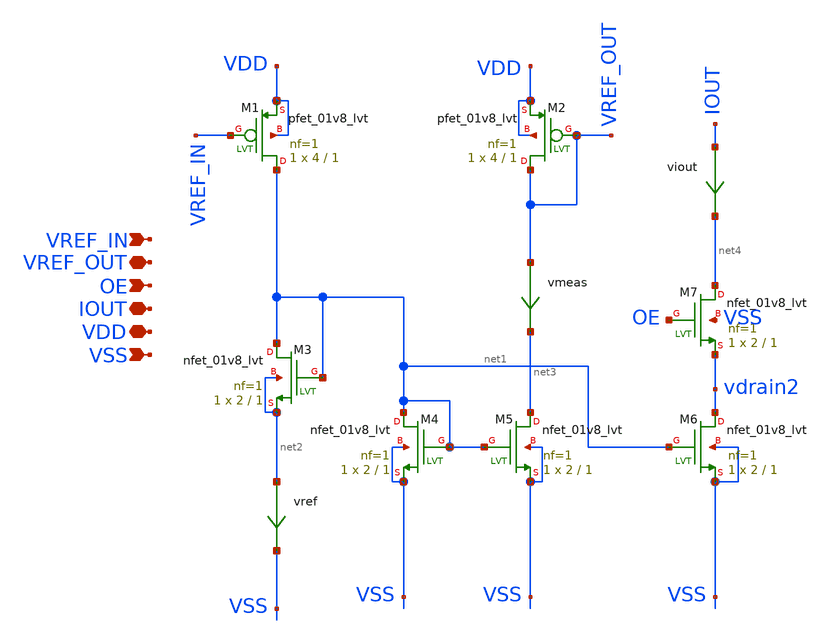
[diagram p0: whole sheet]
** sch_path: tt_um_emilian_rf_playground/xschem/idac1cell.sch
**.subckt idac1cell VSS VREF_OUT VREF_IN VDD IOUT OE
*.ipin VSS
*.iopin VREF_OUT
*.ipin VREF_IN
*.iopin VDD
*.iopin IOUT
*.ipin OE
XM3 net1 net1 net2 net2 sky130_fd_pr__nfet_01v8_lvt L=1 W=2 nf=1 ad='int((nf+1)/2) * W/nf * 0.29' as='int((nf+2)/2) * W/nf * 0.29'
+ pd='2*int((nf+1)/2) * (W/nf + 0.29)' ps='2*int((nf+2)/2) * (W/nf + 0.29)' nrd='0.29 / W' nrs='0.29 / W'
+ sa=0 sb=0 sd=0 mult=1 m=1
XM4 net1 net1 VSS VSS sky130_fd_pr__nfet_01v8_lvt L=1 W=2 nf=1 ad='int((nf+1)/2) * W/nf * 0.29' as='int((nf+2)/2) * W/nf * 0.29'
+ pd='2*int((nf+1)/2) * (W/nf + 0.29)' ps='2*int((nf+2)/2) * (W/nf + 0.29)' nrd='0.29 / W' nrs='0.29 / W'
+ sa=0 sb=0 sd=0 mult=1 m=1
XM1 net1 VREF_IN VDD VDD sky130_fd_pr__pfet_01v8_lvt L=1 W=4 nf=1 ad='int((nf+1)/2) * W/nf * 0.29' as='int((nf+2)/2) * W/nf * 0.29'
+ pd='2*int((nf+1)/2) * (W/nf + 0.29)' ps='2*int((nf+2)/2) * (W/nf + 0.29)' nrd='0.29 / W' nrs='0.29 / W'
+ sa=0 sb=0 sd=0 mult=1 m=1
XM5 net3 net1 VSS VSS sky130_fd_pr__nfet_01v8_lvt L=1 W=2 nf=1 ad='int((nf+1)/2) * W/nf * 0.29' as='int((nf+2)/2) * W/nf * 0.29'
+ pd='2*int((nf+1)/2) * (W/nf + 0.29)' ps='2*int((nf+2)/2) * (W/nf + 0.29)' nrd='0.29 / W' nrs='0.29 / W'
+ sa=0 sb=0 sd=0 mult=1 m=1
XM2 VREF_OUT VREF_OUT VDD VDD sky130_fd_pr__pfet_01v8_lvt L=1 W=4 nf=1 ad='int((nf+1)/2) * W/nf * 0.29'
+ as='int((nf+2)/2) * W/nf * 0.29' pd='2*int((nf+1)/2) * (W/nf + 0.29)' ps='2*int((nf+2)/2) * (W/nf + 0.29)'
+ nrd='0.29 / W' nrs='0.29 / W' sa=0 sb=0 sd=0 mult=1 m=1
XM6 vdrain2 net1 VSS VSS sky130_fd_pr__nfet_01v8_lvt L=1 W=2 nf=1 ad='int((nf+1)/2) * W/nf * 0.29' as='int((nf+2)/2) * W/nf * 0.29'
+ pd='2*int((nf+1)/2) * (W/nf + 0.29)' ps='2*int((nf+2)/2) * (W/nf + 0.29)' nrd='0.29 / W' nrs='0.29 / W'
+ sa=0 sb=0 sd=0 mult=1 m=1
XM7 net4 OE vdrain2 VSS sky130_fd_pr__nfet_01v8_lvt L=1 W=2 nf=1 ad='int((nf+1)/2) * W/nf * 0.29' as='int((nf+2)/2) * W/nf * 0.29'
+ pd='2*int((nf+1)/2) * (W/nf + 0.29)' ps='2*int((nf+2)/2) * (W/nf + 0.29)' nrd='0.29 / W' nrs='0.29 / W'
+ sa=0 sb=0 sd=0 mult=1 m=1
vmeas VREF_OUT net3 0
.save i(vmeas)
viout IOUT net4 0
.save i(viout)
vref net2 VSS 0
.save i(vref)
**.ends
.end
